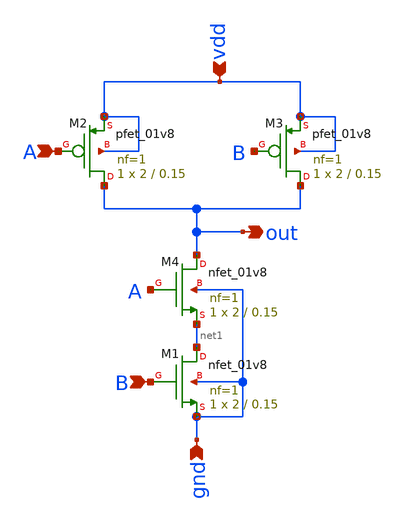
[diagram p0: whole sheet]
** sch_path: schematics/NAND.sch
**.subckt NAND vdd A B out gnd
*.ipin vdd
*.ipin A
*.ipin B
*.opin out
*.ipin gnd
XM1 net1 B gnd gnd sky130_fd_pr__nfet_01v8 L=0.15 W=2 nf=1 ad='int((1 + 1)/2) * 2 / 1 * 0.29' as='int((1 + 2)/2) * 2 / 1 * 0.29'
+ pd='2*int((1 + 1)/2) * (2 / 1 + 0.29)' ps='2*int((1 + 2)/2) * (2 / 1 + 0.29)' nrd='0.29 / 2 ' nrs='0.29 / 2 '
+ sa=0 sb=0 sd=0 mult=1 m=1
XM2 out A vdd vdd sky130_fd_pr__pfet_01v8 L=0.15 W=2 nf=1 ad='int((1 + 1)/2) * 2 / 1 * 0.29' as='int((1 + 2)/2) * 2 / 1 * 0.29'
+ pd='2*int((1 + 1)/2) * (2 / 1 + 0.29)' ps='2*int((1 + 2)/2) * (2 / 1 + 0.29)' nrd='0.29 / 2 ' nrs='0.29 / 2 '
+ sa=0 sb=0 sd=0 mult=1 m=1
XM3 out B vdd vdd sky130_fd_pr__pfet_01v8 L=0.15 W=2 nf=1 ad='int((1 + 1)/2) * 2 / 1 * 0.29' as='int((1 + 2)/2) * 2 / 1 * 0.29'
+ pd='2*int((1 + 1)/2) * (2 / 1 + 0.29)' ps='2*int((1 + 2)/2) * (2 / 1 + 0.29)' nrd='0.29 / 2 ' nrs='0.29 / 2 '
+ sa=0 sb=0 sd=0 mult=1 m=1
XM4 out A net1 gnd sky130_fd_pr__nfet_01v8 L=0.15 W=2 nf=1 ad='int((1 + 1)/2) * 2 / 1 * 0.29' as='int((1 + 2)/2) * 2 / 1 * 0.29'
+ pd='2*int((1 + 1)/2) * (2 / 1 + 0.29)' ps='2*int((1 + 2)/2) * (2 / 1 + 0.29)' nrd='0.29 / 2 ' nrs='0.29 / 2 '
+ sa=0 sb=0 sd=0 mult=1 m=1
**.ends
.end
